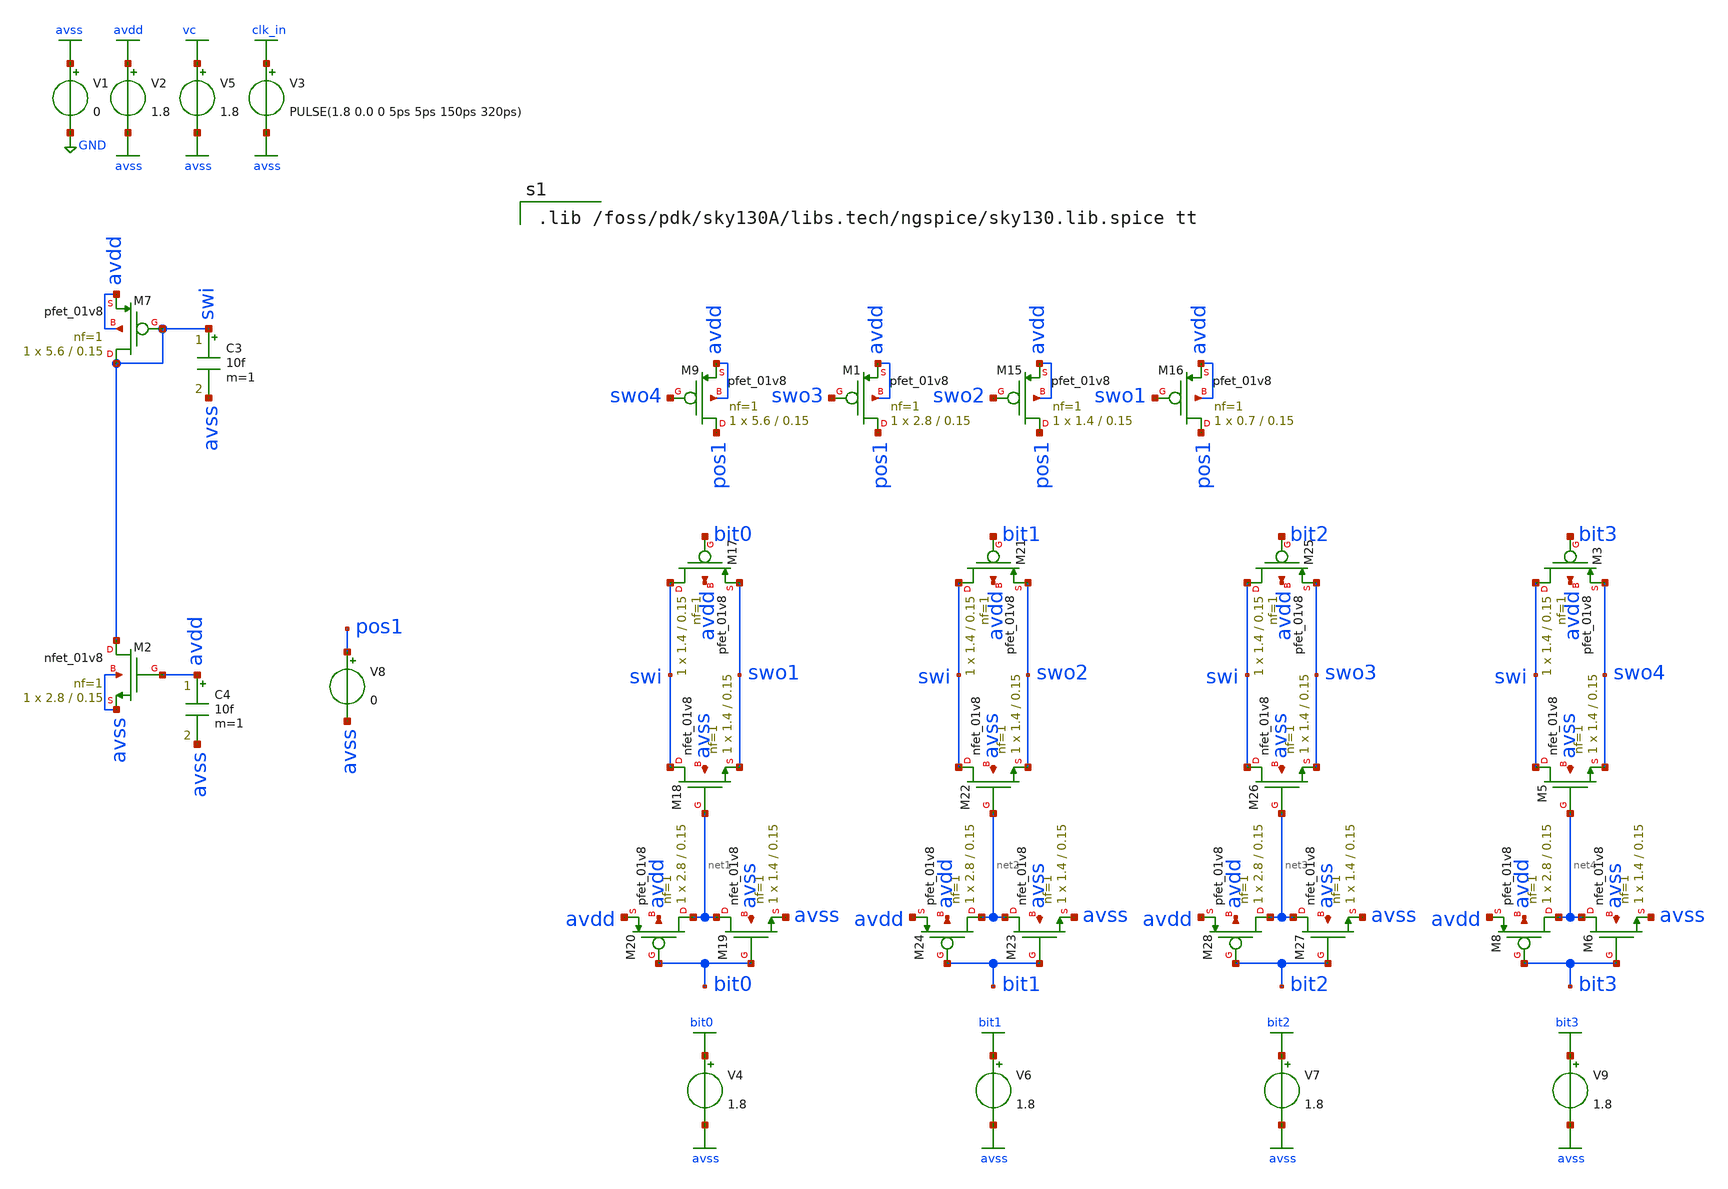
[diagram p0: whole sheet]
** sch_path: xschem/mirror_sim1.sch
**.subckt mirror_sim1
V1 avss GND 0
V2 avdd avss 1.8
V3 clk_in avss PULSE(1.8 0.0 0 5ps 5ps 150ps 320ps)
V5 vc avss 1.8
XM7 swi swi avdd avdd sky130_fd_pr__pfet_01v8 L=0.15 W=5.6 nf=1 ad='int((nf+1)/2) * W/nf * 0.29' as='int((nf+2)/2) * W/nf * 0.29'
+ pd='2*int((nf+1)/2) * (W/nf + 0.29)' ps='2*int((nf+2)/2) * (W/nf + 0.29)' nrd='0.29 / W' nrs='0.29 / W'
+ sa=0 sb=0 sd=0 mult=1 m=1
XM2 swi avdd avss avss sky130_fd_pr__nfet_01v8 L=0.15 W=2.8 nf=1 ad='int((nf+1)/2) * W/nf * 0.29' as='int((nf+2)/2) * W/nf * 0.29'
+ pd='2*int((nf+1)/2) * (W/nf + 0.29)' ps='2*int((nf+2)/2) * (W/nf + 0.29)' nrd='0.29 / W' nrs='0.29 / W'
+ sa=0 sb=0 sd=0 mult=1 m=1
C3 swi avss 10f m=1
C4 avdd avss 10f m=1
XM1 pos1 swo3 avdd avdd sky130_fd_pr__pfet_01v8 L=0.15 W=2.8 nf=1 ad='int((nf+1)/2) * W/nf * 0.29' as='int((nf+2)/2) * W/nf * 0.29'
+ pd='2*int((nf+1)/2) * (W/nf + 0.29)' ps='2*int((nf+2)/2) * (W/nf + 0.29)' nrd='0.29 / W' nrs='0.29 / W'
+ sa=0 sb=0 sd=0 mult=1 m=1
XM15 pos1 swo2 avdd avdd sky130_fd_pr__pfet_01v8 L=0.15 W=1.4 nf=1 ad='int((nf+1)/2) * W/nf * 0.29' as='int((nf+2)/2) * W/nf * 0.29'
+ pd='2*int((nf+1)/2) * (W/nf + 0.29)' ps='2*int((nf+2)/2) * (W/nf + 0.29)' nrd='0.29 / W' nrs='0.29 / W'
+ sa=0 sb=0 sd=0 mult=1 m=1
XM16 pos1 swo1 avdd avdd sky130_fd_pr__pfet_01v8 L=0.15 W=0.7 nf=1 ad='int((nf+1)/2) * W/nf * 0.29' as='int((nf+2)/2) * W/nf * 0.29'
+ pd='2*int((nf+1)/2) * (W/nf + 0.29)' ps='2*int((nf+2)/2) * (W/nf + 0.29)' nrd='0.29 / W' nrs='0.29 / W'
+ sa=0 sb=0 sd=0 mult=1 m=1
XM17 swi bit0 swo1 avdd sky130_fd_pr__pfet_01v8 L=0.15 W=1.4 nf=1 ad='int((nf+1)/2) * W/nf * 0.29' as='int((nf+2)/2) * W/nf * 0.29'
+ pd='2*int((nf+1)/2) * (W/nf + 0.29)' ps='2*int((nf+2)/2) * (W/nf + 0.29)' nrd='0.29 / W' nrs='0.29 / W'
+ sa=0 sb=0 sd=0 mult=1 m=1
XM18 swi net1 swo1 avss sky130_fd_pr__nfet_01v8 L=0.15 W=1.4 nf=1 ad='int((nf+1)/2) * W/nf * 0.29' as='int((nf+2)/2) * W/nf * 0.29'
+ pd='2*int((nf+1)/2) * (W/nf + 0.29)' ps='2*int((nf+2)/2) * (W/nf + 0.29)' nrd='0.29 / W' nrs='0.29 / W'
+ sa=0 sb=0 sd=0 mult=1 m=1
XM19 net1 bit0 avss avss sky130_fd_pr__nfet_01v8 L=0.15 W=1.4 nf=1 ad='int((nf+1)/2) * W/nf * 0.29' as='int((nf+2)/2) * W/nf * 0.29'
+ pd='2*int((nf+1)/2) * (W/nf + 0.29)' ps='2*int((nf+2)/2) * (W/nf + 0.29)' nrd='0.29 / W' nrs='0.29 / W'
+ sa=0 sb=0 sd=0 mult=1 m=1
XM20 net1 bit0 avdd avdd sky130_fd_pr__pfet_01v8 L=0.15 W=2.8 nf=1 ad='int((nf+1)/2) * W/nf * 0.29' as='int((nf+2)/2) * W/nf * 0.29'
+ pd='2*int((nf+1)/2) * (W/nf + 0.29)' ps='2*int((nf+2)/2) * (W/nf + 0.29)' nrd='0.29 / W' nrs='0.29 / W'
+ sa=0 sb=0 sd=0 mult=1 m=1
XM21 swi bit1 swo2 avdd sky130_fd_pr__pfet_01v8 L=0.15 W=1.4 nf=1 ad='int((nf+1)/2) * W/nf * 0.29' as='int((nf+2)/2) * W/nf * 0.29'
+ pd='2*int((nf+1)/2) * (W/nf + 0.29)' ps='2*int((nf+2)/2) * (W/nf + 0.29)' nrd='0.29 / W' nrs='0.29 / W'
+ sa=0 sb=0 sd=0 mult=1 m=1
XM22 swi net2 swo2 avss sky130_fd_pr__nfet_01v8 L=0.15 W=1.4 nf=1 ad='int((nf+1)/2) * W/nf * 0.29' as='int((nf+2)/2) * W/nf * 0.29'
+ pd='2*int((nf+1)/2) * (W/nf + 0.29)' ps='2*int((nf+2)/2) * (W/nf + 0.29)' nrd='0.29 / W' nrs='0.29 / W'
+ sa=0 sb=0 sd=0 mult=1 m=1
XM23 net2 bit1 avss avss sky130_fd_pr__nfet_01v8 L=0.15 W=1.4 nf=1 ad='int((nf+1)/2) * W/nf * 0.29' as='int((nf+2)/2) * W/nf * 0.29'
+ pd='2*int((nf+1)/2) * (W/nf + 0.29)' ps='2*int((nf+2)/2) * (W/nf + 0.29)' nrd='0.29 / W' nrs='0.29 / W'
+ sa=0 sb=0 sd=0 mult=1 m=1
XM24 net2 bit1 avdd avdd sky130_fd_pr__pfet_01v8 L=0.15 W=2.8 nf=1 ad='int((nf+1)/2) * W/nf * 0.29' as='int((nf+2)/2) * W/nf * 0.29'
+ pd='2*int((nf+1)/2) * (W/nf + 0.29)' ps='2*int((nf+2)/2) * (W/nf + 0.29)' nrd='0.29 / W' nrs='0.29 / W'
+ sa=0 sb=0 sd=0 mult=1 m=1
XM25 swi bit2 swo3 avdd sky130_fd_pr__pfet_01v8 L=0.15 W=1.4 nf=1 ad='int((nf+1)/2) * W/nf * 0.29' as='int((nf+2)/2) * W/nf * 0.29'
+ pd='2*int((nf+1)/2) * (W/nf + 0.29)' ps='2*int((nf+2)/2) * (W/nf + 0.29)' nrd='0.29 / W' nrs='0.29 / W'
+ sa=0 sb=0 sd=0 mult=1 m=1
XM26 swi net3 swo3 avss sky130_fd_pr__nfet_01v8 L=0.15 W=1.4 nf=1 ad='int((nf+1)/2) * W/nf * 0.29' as='int((nf+2)/2) * W/nf * 0.29'
+ pd='2*int((nf+1)/2) * (W/nf + 0.29)' ps='2*int((nf+2)/2) * (W/nf + 0.29)' nrd='0.29 / W' nrs='0.29 / W'
+ sa=0 sb=0 sd=0 mult=1 m=1
XM27 net3 bit2 avss avss sky130_fd_pr__nfet_01v8 L=0.15 W=1.4 nf=1 ad='int((nf+1)/2) * W/nf * 0.29' as='int((nf+2)/2) * W/nf * 0.29'
+ pd='2*int((nf+1)/2) * (W/nf + 0.29)' ps='2*int((nf+2)/2) * (W/nf + 0.29)' nrd='0.29 / W' nrs='0.29 / W'
+ sa=0 sb=0 sd=0 mult=1 m=1
XM28 net3 bit2 avdd avdd sky130_fd_pr__pfet_01v8 L=0.15 W=2.8 nf=1 ad='int((nf+1)/2) * W/nf * 0.29' as='int((nf+2)/2) * W/nf * 0.29'
+ pd='2*int((nf+1)/2) * (W/nf + 0.29)' ps='2*int((nf+2)/2) * (W/nf + 0.29)' nrd='0.29 / W' nrs='0.29 / W'
+ sa=0 sb=0 sd=0 mult=1 m=1
V4 bit0 avss 1.8
V6 bit1 avss 1.8
V7 bit2 avss 1.8
V8 pos1 avss 0
XM3 swi bit3 swo4 avdd sky130_fd_pr__pfet_01v8 L=0.15 W=1.4 nf=1 ad='int((nf+1)/2) * W/nf * 0.29' as='int((nf+2)/2) * W/nf * 0.29'
+ pd='2*int((nf+1)/2) * (W/nf + 0.29)' ps='2*int((nf+2)/2) * (W/nf + 0.29)' nrd='0.29 / W' nrs='0.29 / W'
+ sa=0 sb=0 sd=0 mult=1 m=1
XM5 swi net4 swo4 avss sky130_fd_pr__nfet_01v8 L=0.15 W=1.4 nf=1 ad='int((nf+1)/2) * W/nf * 0.29' as='int((nf+2)/2) * W/nf * 0.29'
+ pd='2*int((nf+1)/2) * (W/nf + 0.29)' ps='2*int((nf+2)/2) * (W/nf + 0.29)' nrd='0.29 / W' nrs='0.29 / W'
+ sa=0 sb=0 sd=0 mult=1 m=1
XM6 net4 bit3 avss avss sky130_fd_pr__nfet_01v8 L=0.15 W=1.4 nf=1 ad='int((nf+1)/2) * W/nf * 0.29' as='int((nf+2)/2) * W/nf * 0.29'
+ pd='2*int((nf+1)/2) * (W/nf + 0.29)' ps='2*int((nf+2)/2) * (W/nf + 0.29)' nrd='0.29 / W' nrs='0.29 / W'
+ sa=0 sb=0 sd=0 mult=1 m=1
XM8 net4 bit3 avdd avdd sky130_fd_pr__pfet_01v8 L=0.15 W=2.8 nf=1 ad='int((nf+1)/2) * W/nf * 0.29' as='int((nf+2)/2) * W/nf * 0.29'
+ pd='2*int((nf+1)/2) * (W/nf + 0.29)' ps='2*int((nf+2)/2) * (W/nf + 0.29)' nrd='0.29 / W' nrs='0.29 / W'
+ sa=0 sb=0 sd=0 mult=1 m=1
V9 bit3 avss 1.8
XM9 pos1 swo4 avdd avdd sky130_fd_pr__pfet_01v8 L=0.15 W=5.6 nf=1 ad='int((nf+1)/2) * W/nf * 0.29' as='int((nf+2)/2) * W/nf * 0.29'
+ pd='2*int((nf+1)/2) * (W/nf + 0.29)' ps='2*int((nf+2)/2) * (W/nf + 0.29)' nrd='0.29 / W' nrs='0.29 / W'
+ sa=0 sb=0 sd=0 mult=1 m=1
**** begin user architecture code

.lib /foss/pdk/sky130A/libs.tech/ngspice/sky130.lib.spice tt












.control
set temp=25
alter v4 0
alter v6 0
alter v7 0
alter v9 0
save clk_in vc @V1[i] @V8[i]
tran 0.01n 50n 20n
run
*plot clk_out clk_in
plot @V8[i]
*plot tran1.clk_out tran2.clk_out tran3.clk_out tran4.clk_out tran5.clk_out tran6.clk_out
*+ tran7.clk_out tran8.clk_out xlimit 49ns 50ns
*plot tran1.s1 tran2.s1 tran3.s1 tran4.s1 tran5.s1 tran6.s1 tran7.s1 tran8.s1 tran9.s1 tran10.s1
*+ xlimit 49ns 50ns
*plot tran1.@V1[i] tran5.@V1[i] tran10.@V1[i]
.endc
.end


**** end user architecture code
**.ends
.GLOBAL avdd
.GLOBAL avss
.GLOBAL GND
.GLOBAL vc
.GLOBAL clk_in
.GLOBAL bit0
.GLOBAL bit1
.GLOBAL bit2
.GLOBAL bit3
.end
